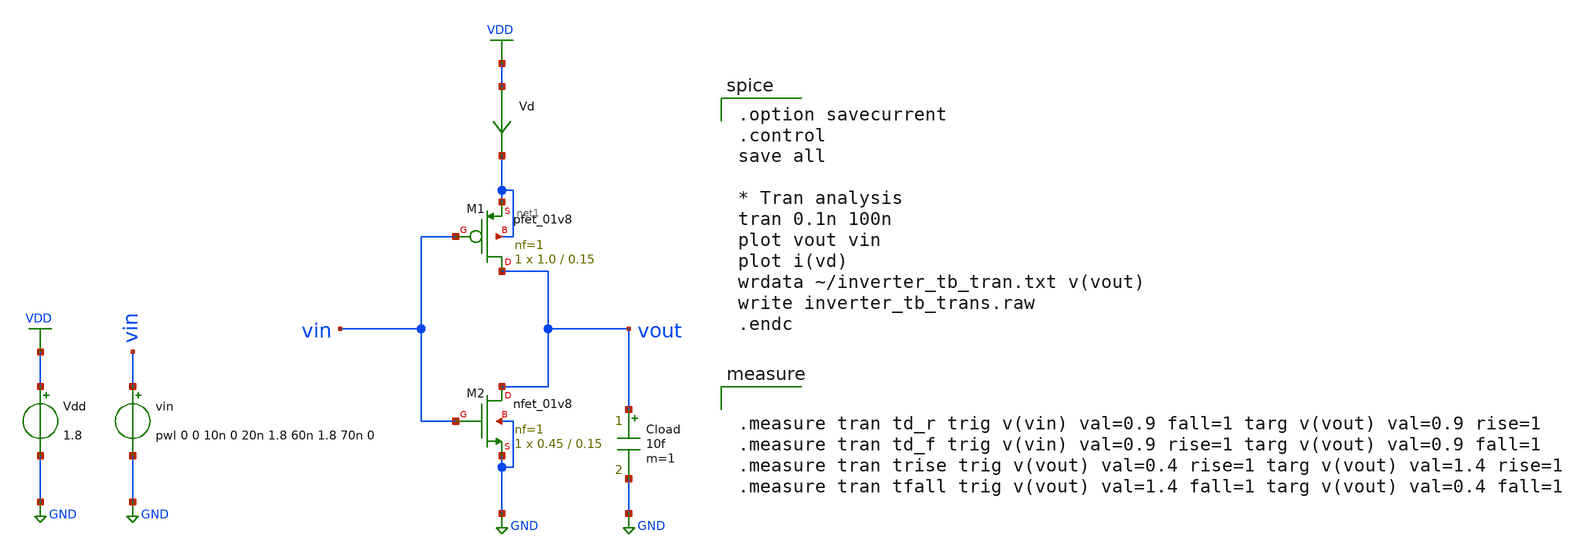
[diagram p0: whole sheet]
** sch_path: samples/inverter/SKY130/inverter_tb_trans.sch
**.subckt inverter_tb_trans
Vdd VDD GND 1.8
vin vin GND pwl 0 0 10n 0 20n 1.8 60n 1.8 70n 0
Vd VDD net1 0
.save i(vd)
Cload vout GND 10f m=1
XM1 vout vin net1 net1 sky130_fd_pr__pfet_01v8 L=0.15 W=1.0 nf=1 ad='int((1 + 1)/2) * 1.0 / 1 * 0.29'
+ as='int((1 + 2)/2) * 1.0 / 1 * 0.29' pd='2*int((1 + 1)/2) * (1.0 / 1 + 0.29)' ps='2*int((1 + 2)/2) * (1.0 / 1 + 0.29)'
+ nrd='0.29 / 1.0 ' nrs='0.29 / 1.0 ' sa=0 sb=0 sd=0 mult=1 m=1
XM2 vout vin GND GND sky130_fd_pr__nfet_01v8 L=0.15 W=0.45 nf=1 ad='int((1 + 1)/2) * 0.45 / 1 * 0.29'
+ as='int((1 + 2)/2) * 0.45 / 1 * 0.29' pd='2*int((1 + 1)/2) * (0.45 / 1 + 0.29)' ps='2*int((1 + 2)/2) * (0.45 / 1 + 0.29)'
+ nrd='0.29 / 0.45 ' nrs='0.29 / 0.45 ' sa=0 sb=0 sd=0 mult=1 m=1
**** begin user architecture code

.option savecurrent
.control
save all

* Tran analysis
tran 0.1n 100n
plot vout vin
plot i(vd)
wrdata ~/inverter_tb_tran.txt v(vout)
write inverter_tb_trans.raw
.endc



.measure tran td_r trig v(vin) val=0.9 fall=1 targ v(vout) val=0.9 rise=1
.measure tran td_f trig v(vin) val=0.9 rise=1 targ v(vout) val=0.9 fall=1
.measure tran trise trig v(vout) val=0.4 rise=1 targ v(vout) val=1.4 rise=1
.measure tran tfall trig v(vout) val=1.4 fall=1 targ v(vout) val=0.4 fall=1



** opencircuitdesign pdks install
.lib $::SKYWATER_MODELS/sky130.lib.spice tt

**** end user architecture code
**.ends
.GLOBAL VDD
.GLOBAL GND
.end
